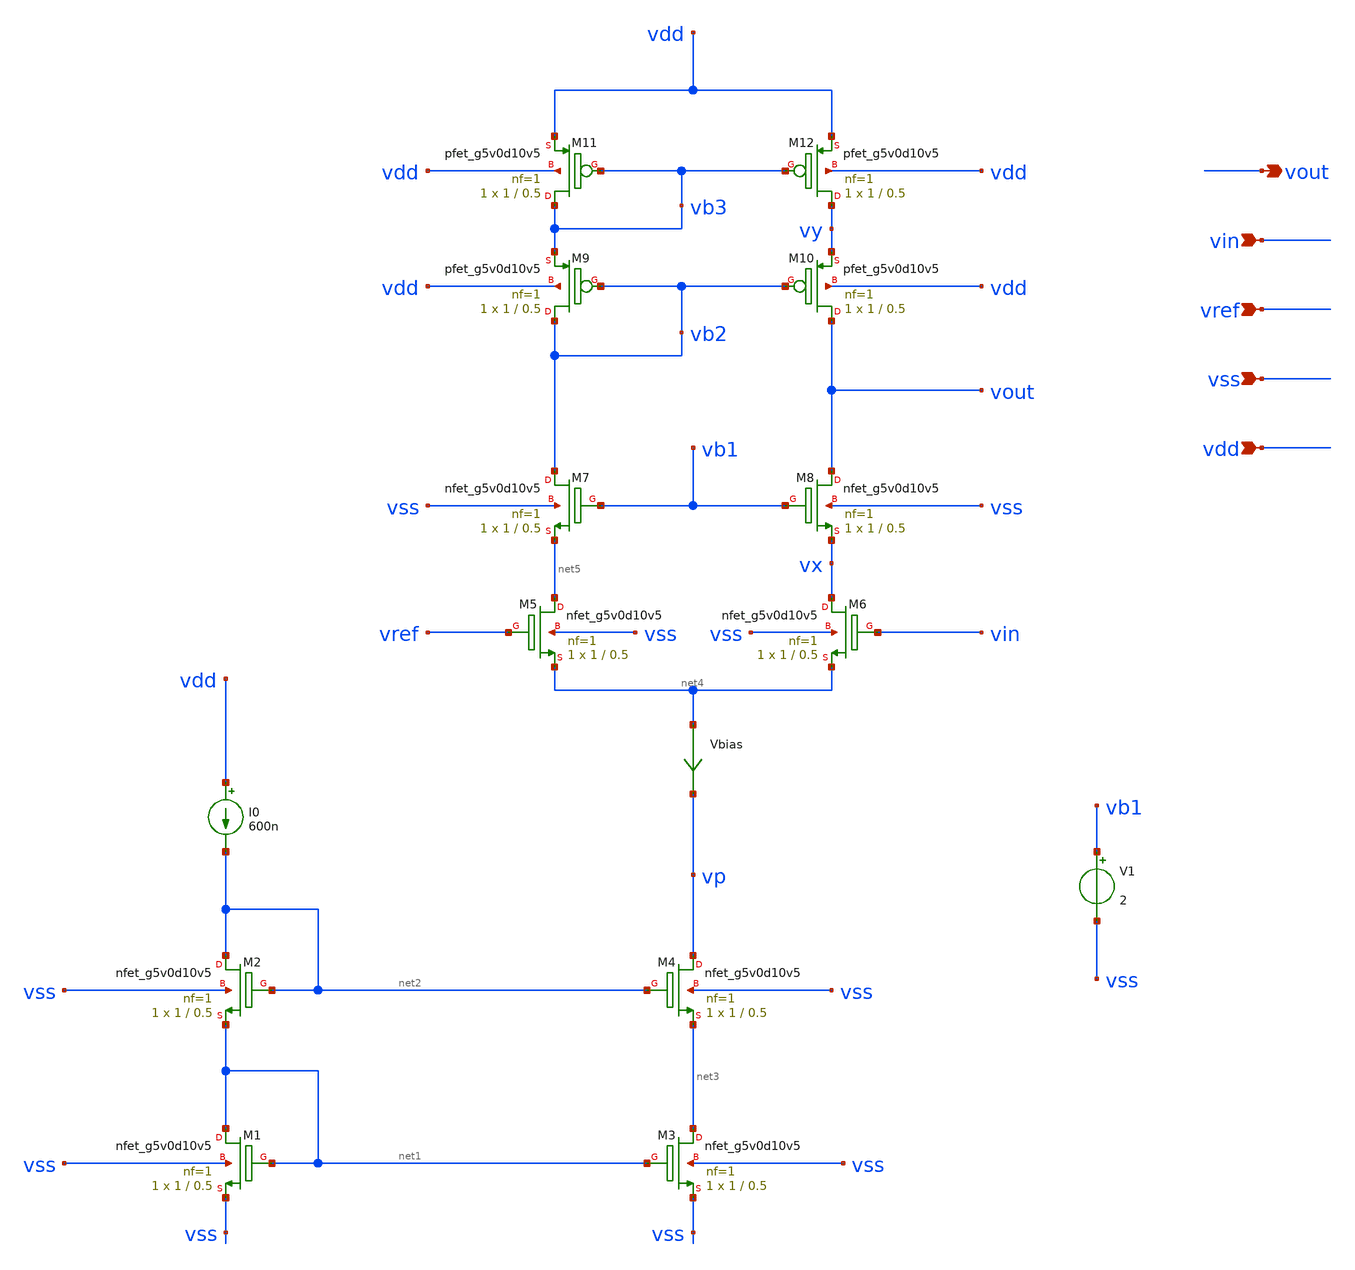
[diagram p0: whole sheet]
** sch_path: xschem/cascode_opamp.sch
**.subckt cascode_opamp vin vref vss vout vdd
*.ipin vin
*.ipin vref
*.ipin vss
*.opin vout
*.ipin vdd
I0 vdd net2 600n
XM1 net1 net1 vss vss sky130_fd_pr__nfet_g5v0d10v5 L=0.5 W=1 nf=1 ad='int((nf+1)/2) * W/nf * 0.29' as='int((nf+2)/2) * W/nf * 0.29'
+ pd='2*int((nf+1)/2) * (W/nf + 0.29)' ps='2*int((nf+2)/2) * (W/nf + 0.29)' nrd='0.29 / W' nrs='0.29 / W'
+ sa=0 sb=0 sd=0 mult=1 m=1
XM2 net2 net2 net1 vss sky130_fd_pr__nfet_g5v0d10v5 L=0.5 W=1 nf=1 ad='int((nf+1)/2) * W/nf * 0.29' as='int((nf+2)/2) * W/nf * 0.29'
+ pd='2*int((nf+1)/2) * (W/nf + 0.29)' ps='2*int((nf+2)/2) * (W/nf + 0.29)' nrd='0.29 / W' nrs='0.29 / W'
+ sa=0 sb=0 sd=0 mult=1 m=1
XM3 net3 net1 vss vss sky130_fd_pr__nfet_g5v0d10v5 L=0.5 W=1 nf=1 ad='int((nf+1)/2) * W/nf * 0.29' as='int((nf+2)/2) * W/nf * 0.29'
+ pd='2*int((nf+1)/2) * (W/nf + 0.29)' ps='2*int((nf+2)/2) * (W/nf + 0.29)' nrd='0.29 / W' nrs='0.29 / W'
+ sa=0 sb=0 sd=0 mult=1 m=1
XM4 vp net2 net3 vss sky130_fd_pr__nfet_g5v0d10v5 L=0.5 W=1 nf=1 ad='int((nf+1)/2) * W/nf * 0.29' as='int((nf+2)/2) * W/nf * 0.29'
+ pd='2*int((nf+1)/2) * (W/nf + 0.29)' ps='2*int((nf+2)/2) * (W/nf + 0.29)' nrd='0.29 / W' nrs='0.29 / W'
+ sa=0 sb=0 sd=0 mult=1 m=1
XM5 net5 vref net4 vss sky130_fd_pr__nfet_g5v0d10v5 L=0.5 W=1 nf=1 ad='int((nf+1)/2) * W/nf * 0.29' as='int((nf+2)/2) * W/nf * 0.29'
+ pd='2*int((nf+1)/2) * (W/nf + 0.29)' ps='2*int((nf+2)/2) * (W/nf + 0.29)' nrd='0.29 / W' nrs='0.29 / W'
+ sa=0 sb=0 sd=0 mult=1 m=1
XM6 vx vin net4 vss sky130_fd_pr__nfet_g5v0d10v5 L=0.5 W=1 nf=1 ad='int((nf+1)/2) * W/nf * 0.29' as='int((nf+2)/2) * W/nf * 0.29'
+ pd='2*int((nf+1)/2) * (W/nf + 0.29)' ps='2*int((nf+2)/2) * (W/nf + 0.29)' nrd='0.29 / W' nrs='0.29 / W'
+ sa=0 sb=0 sd=0 mult=1 m=1
XM7 vb2 vb1 net5 vss sky130_fd_pr__nfet_g5v0d10v5 L=0.5 W=1 nf=1 ad='int((nf+1)/2) * W/nf * 0.29' as='int((nf+2)/2) * W/nf * 0.29'
+ pd='2*int((nf+1)/2) * (W/nf + 0.29)' ps='2*int((nf+2)/2) * (W/nf + 0.29)' nrd='0.29 / W' nrs='0.29 / W'
+ sa=0 sb=0 sd=0 mult=1 m=1
XM8 vout vb1 vx vss sky130_fd_pr__nfet_g5v0d10v5 L=0.5 W=1 nf=1 ad='int((nf+1)/2) * W/nf * 0.29' as='int((nf+2)/2) * W/nf * 0.29'
+ pd='2*int((nf+1)/2) * (W/nf + 0.29)' ps='2*int((nf+2)/2) * (W/nf + 0.29)' nrd='0.29 / W' nrs='0.29 / W'
+ sa=0 sb=0 sd=0 mult=1 m=1
XM9 vb2 vb2 vb3 vdd sky130_fd_pr__pfet_g5v0d10v5 L=0.5 W=1 nf=1 ad='int((nf+1)/2) * W/nf * 0.29' as='int((nf+2)/2) * W/nf * 0.29'
+ pd='2*int((nf+1)/2) * (W/nf + 0.29)' ps='2*int((nf+2)/2) * (W/nf + 0.29)' nrd='0.29 / W' nrs='0.29 / W'
+ sa=0 sb=0 sd=0 mult=1 m=1
XM10 vout vb2 vy vdd sky130_fd_pr__pfet_g5v0d10v5 L=0.5 W=1 nf=1 ad='int((nf+1)/2) * W/nf * 0.29' as='int((nf+2)/2) * W/nf * 0.29'
+ pd='2*int((nf+1)/2) * (W/nf + 0.29)' ps='2*int((nf+2)/2) * (W/nf + 0.29)' nrd='0.29 / W' nrs='0.29 / W'
+ sa=0 sb=0 sd=0 mult=1 m=1
XM11 vb3 vb3 vdd vdd sky130_fd_pr__pfet_g5v0d10v5 L=0.5 W=1 nf=1 ad='int((nf+1)/2) * W/nf * 0.29' as='int((nf+2)/2) * W/nf * 0.29'
+ pd='2*int((nf+1)/2) * (W/nf + 0.29)' ps='2*int((nf+2)/2) * (W/nf + 0.29)' nrd='0.29 / W' nrs='0.29 / W'
+ sa=0 sb=0 sd=0 mult=1 m=1
XM12 vy vb3 vdd vdd sky130_fd_pr__pfet_g5v0d10v5 L=0.5 W=1 nf=1 ad='int((nf+1)/2) * W/nf * 0.29' as='int((nf+2)/2) * W/nf * 0.29'
+ pd='2*int((nf+1)/2) * (W/nf + 0.29)' ps='2*int((nf+2)/2) * (W/nf + 0.29)' nrd='0.29 / W' nrs='0.29 / W'
+ sa=0 sb=0 sd=0 mult=1 m=1
Vbias net4 vp 0
.save i(vbias)
V1 vb1 vss 2
**.ends
.end
